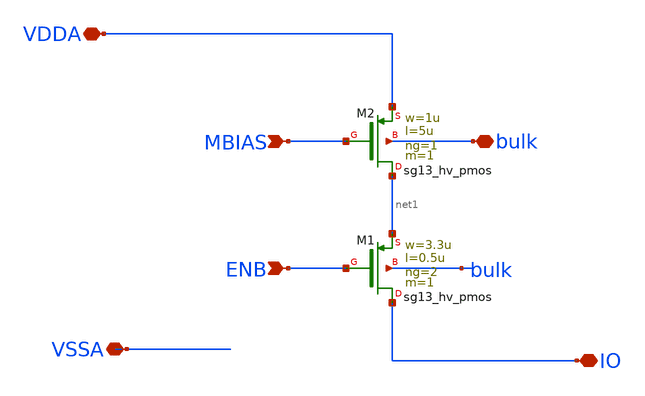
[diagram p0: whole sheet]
** sch_path: ISOURCE.sch
**.subckt ISOURCE VDDA MBIAS ENB IO VSSA bulk
*.iopin VDDA
*.ipin MBIAS
*.ipin ENB
*.iopin IO
*.iopin VSSA
*.iopin bulk
X[2:1]M2 net1 MBIAS VDDA bulk sg13_hv_pmos w=1u l=5u ng=1 m=1 mm_ok=1
X[2:1]M1 IO ENB net1 bulk sg13_hv_pmos w=3.3u l=0.5u ng=2 m=1 mm_ok=1
**.ends
.end
